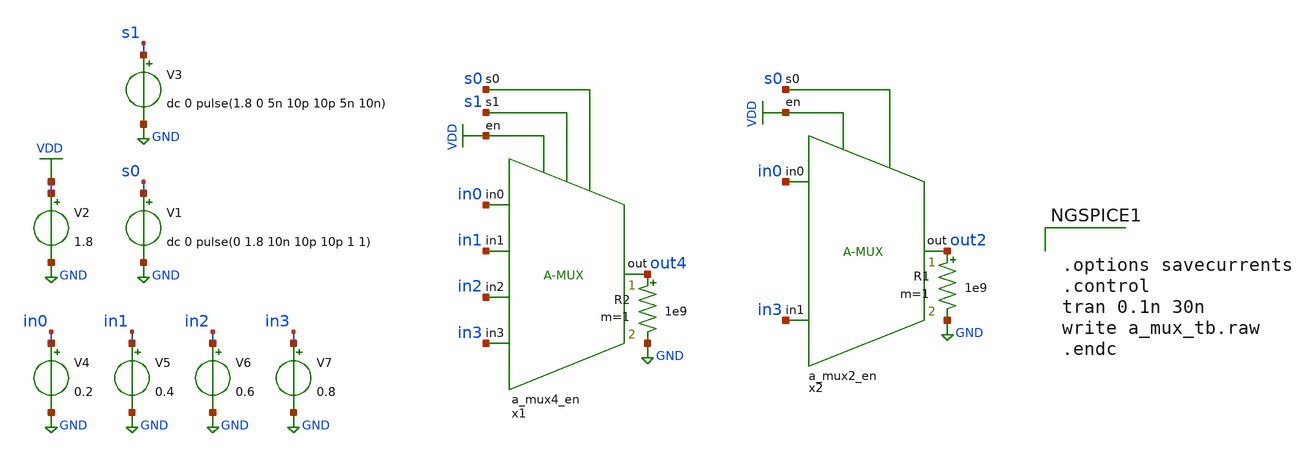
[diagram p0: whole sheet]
** sch_path: verification/schematic_sim/a_mux_tb.sch
**.subckt a_mux_tb
V2 VDD GND 1.8
V1 s0 GND dc 0 pulse(0 1.8 10n 10p 10p 1 1)
V3 s1 GND dc 0 pulse(1.8 0 5n 10p 10p 5n 10n)
V4 in0 GND 0.2
V5 in1 GND 0.4
V6 in2 GND 0.6
V7 in3 GND 0.8
R1 out2 GND 1e9 m=1
x1 s0 s1 VDD in0 in1 in2 in3 out4 VDD GND a_mux4_en
x2 s0 VDD in0 in3 out2 VDD VSS a_mux2_en
R2 out4 GND 1e9 m=1
**** begin user architecture code


.options savecurrents
.control
tran 0.1n 30n
write a_mux_tb.raw
.endc



** opencircuitdesign pdks install
.lib /farmshare/home/classes/ee/372/PDKs/open_pdks_1.0.310/sky130/sky130A/libs.tech/ngspice/sky130.lib.spice tt
.inc /farmshare/home/classes/ee/372/PDKs/open_pdks_1.0.310/sky130/sky130A/libs.ref/sky130_fd_sc_hd/spice/sky130_fd_sc_hd.spice

**** end user architecture code
**.ends

* expanding   symbol:  a_mux4_en.sym # of pins=8
** sym_path: design/analog_modulator/schematic/a_mux4_en.sym
** sch_path: design/analog_modulator/schematic/a_mux4_en.sch
.subckt a_mux4_en s0 s1 en in0 in1 in2 in3 out VDD VSS
*.ipin en
*.ipin s1
*.ipin s0
*.ipin in0
*.ipin in1
*.ipin in2
*.ipin in3
*.opin out
x1 net4 out net5 en3_b VDD VSS switch_5t
x2 net3 out net6 en2_b VDD VSS switch_5t
x3 net2 out net7 en1_b VDD VSS switch_5t
x4 net1 out net8 en0_b VDD VSS switch_5t
x5 en3_b VSS VSS VDD VDD net5 sky130_fd_sc_hd__inv_1
x6 en2_b VSS VSS VDD VDD net6 sky130_fd_sc_hd__inv_1
x7 en1_b VSS VSS VDD VDD net7 sky130_fd_sc_hd__inv_1
x8 en0_b VSS VSS VDD VDD net8 sky130_fd_sc_hd__inv_1
x13 s0 VSS VSS VDD VDD s0_b sky130_fd_sc_hd__inv_1
x14 s1 VSS VSS VDD VDD s1_b sky130_fd_sc_hd__inv_1
x9 s1_b s0_b VSS VSS VDD VDD en0_b sky130_fd_sc_hd__nand2_1
x10 s1 s0_b VSS VSS VDD VDD en1_b sky130_fd_sc_hd__nand2_1
x11 s0 s1_b VSS VSS VDD VDD en2_b sky130_fd_sc_hd__nand2_1
x12 s0 s1 VSS VSS VDD VDD en3_b sky130_fd_sc_hd__nand2_1
x15 in0 net1 en en_b VDD VSS 1 5.3 0.15 13.7 0.15 transmission_gate
x16 in1 net2 en en_b VDD VSS 1 5.3 0.15 13.7 0.15 transmission_gate
x17 in2 net3 en en_b VDD VSS 1 5.3 0.15 13.7 0.15 transmission_gate
x18 in3 net4 en en_b VDD VSS 1 5.3 0.15 13.7 0.15 transmission_gate
x19 en VSS VSS VDD VDD en_b sky130_fd_sc_hd__inv_1
.ends


* expanding   symbol:  a_mux2_en.sym # of pins=5
** sym_path: design/analog_modulator/schematic/a_mux2_en.sym
** sch_path: design/analog_modulator/schematic/a_mux2_en.sch
.subckt a_mux2_en s0 en in0 in1 out VDD VSS
*.ipin en
*.ipin s0
*.ipin in0
*.ipin in1
*.opin out
x3 net2 out s0 s0_b VDD VSS switch_5t
x4 net1 out s0_b s0 VDD VSS switch_5t
x15 in0 net1 en en_b VDD VSS 1 5.3 0.15 13.7 0.15 transmission_gate
x16 in1 net2 en en_b VDD VSS 1 5.3 0.15 13.7 0.15 transmission_gate
x19 en VSS VSS VDD VDD en_b sky130_fd_sc_hd__inv_1
x1 s0 VSS VSS VDD VDD s0_b sky130_fd_sc_hd__inv_1
.ends


* expanding   symbol:  switch_5t.sym # of pins=4
** sym_path: design/analog_modulator/schematic/switch_5t.sym
** sch_path: design/analog_modulator/schematic/switch_5t.sch
.subckt switch_5t in out en en_b VDD VSS
*.iopin in
*.iopin out
*.ipin en
*.ipin en_b
x1 in net1 en en_b VDD VSS 1 5.3 0.15 13.7 0.15 transmission_gate
x2 net1 out en en_b VDD VSS 1 5.3 0.15 13.7 0.15 transmission_gate
XM1 net1 en_b VSS VSS sky130_fd_pr__nfet_01v8 L=0.15 W=0.5 nf=1 ad='int((nf+1)/2) * W/nf * 0.29' as='int((nf+2)/2) * W/nf * 0.29'
+ pd='2*int((nf+1)/2) * (W/nf + 0.29)' ps='2*int((nf+2)/2) * (W/nf + 0.29)' nrd='0.29 / W' nrs='0.29 / W'
+ sa=0 sb=0 sd=0 mult=1 m=1
.ends


* expanding   symbol:  transmission_gate.sym # of pins=4
** sym_path: design/analog_modulator/schematic/transmission_gate.sym
** sch_path: design/analog_modulator/schematic/transmission_gate.sch
.subckt transmission_gate in out en en_b VDD VSS N W_N L_N W_P L_P    N=1 W_N=5.3 L_N=0.15 W_P=13.7
+ L_P=0.15
*.iopin in
*.iopin out
*.ipin en
*.ipin en_b
XM1 out en in VSS sky130_fd_pr__nfet_01v8 L='L_N' W='W_N' nf=1 ad='int((nf+1)/2) * W/nf * 0.29' as='int((nf+2)/2) * W/nf * 0.29'
+ pd='2*int((nf+1)/2) * (W/nf + 0.29)' ps='2*int((nf+2)/2) * (W/nf + 0.29)' nrd='0.29 / W' nrs='0.29 / W'
+ sa=0 sb=0 sd=0 mult='N' m='N'
XM2 out en_b in VDD sky130_fd_pr__pfet_01v8 L='L_P' W='W_P' nf=1 ad='int((nf+1)/2) * W/nf * 0.29' as='int((nf+2)/2) * W/nf * 0.29'
+ pd='2*int((nf+1)/2) * (W/nf + 0.29)' ps='2*int((nf+2)/2) * (W/nf + 0.29)' nrd='0.29 / W' nrs='0.29 / W'
+ sa=0 sb=0 sd=0 mult='N' m='N'
.ends

.GLOBAL GND
.GLOBAL VDD
.end
